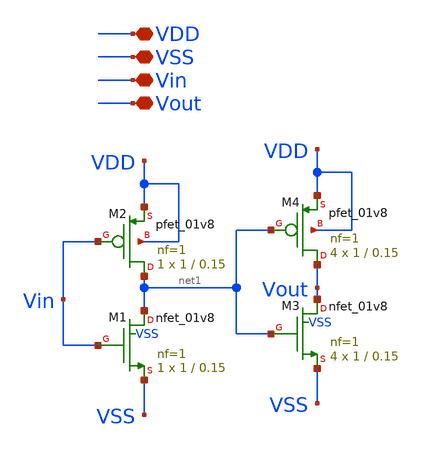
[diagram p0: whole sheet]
** sch_path: Buffer/Buffer.sch
**.subckt Buffer VDD Vin Vout VSS
*.iopin VDD
*.iopin Vin
*.iopin Vout
*.iopin VSS
XM1 net1 Vin VSS VSS sky130_fd_pr__nfet_01v8 L=0.15 W=1 nf=1 ad='int((nf+1)/2) * W/nf * 0.29' as='int((nf+2)/2) * W/nf * 0.29'
+ pd='2*int((nf+1)/2) * (W/nf + 0.29)' ps='2*int((nf+2)/2) * (W/nf + 0.29)' nrd='0.29 / W' nrs='0.29 / W'
+ sa=0 sb=0 sd=0 mult=1 m=1
XM2 net1 Vin VDD VDD sky130_fd_pr__pfet_01v8 L=0.15 W=1 nf=1 ad='int((nf+1)/2) * W/nf * 0.29' as='int((nf+2)/2) * W/nf * 0.29'
+ pd='2*int((nf+1)/2) * (W/nf + 0.29)' ps='2*int((nf+2)/2) * (W/nf + 0.29)' nrd='0.29 / W' nrs='0.29 / W'
+ sa=0 sb=0 sd=0 mult=1 m=1
XM3 Vout net1 VSS VSS sky130_fd_pr__nfet_01v8 L=0.15 W=1 nf=1 ad='int((nf+1)/2) * W/nf * 0.29' as='int((nf+2)/2) * W/nf * 0.29'
+ pd='2*int((nf+1)/2) * (W/nf + 0.29)' ps='2*int((nf+2)/2) * (W/nf + 0.29)' nrd='0.29 / W' nrs='0.29 / W'
+ sa=0 sb=0 sd=0 mult=4 m=4
XM4 Vout net1 VDD VDD sky130_fd_pr__pfet_01v8 L=0.15 W=1 nf=1 ad='int((nf+1)/2) * W/nf * 0.29' as='int((nf+2)/2) * W/nf * 0.29'
+ pd='2*int((nf+1)/2) * (W/nf + 0.29)' ps='2*int((nf+2)/2) * (W/nf + 0.29)' nrd='0.29 / W' nrs='0.29 / W'
+ sa=0 sb=0 sd=0 mult=4 m=4
**.ends
.end
